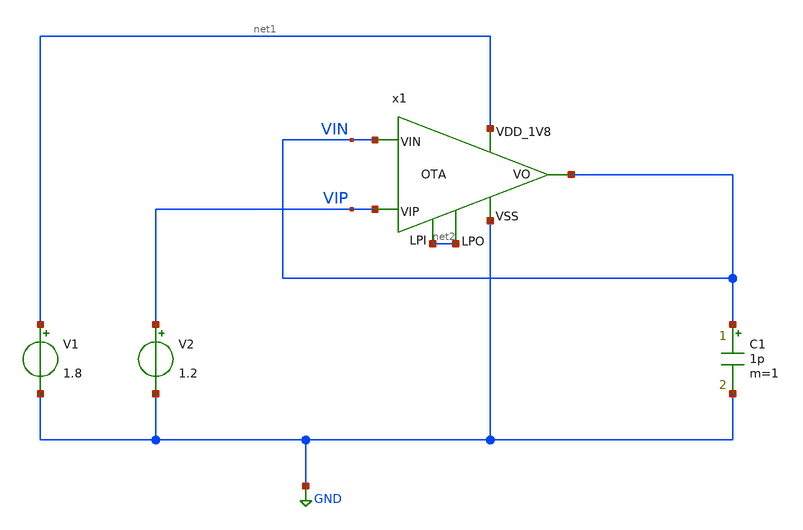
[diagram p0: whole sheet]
** sch_path: design/OTA_SKY130NM/TB_OTA.sch
**.subckt TB_OTA
V2 VIP GND 1.2
C1 VIN GND 1p m=1
V1 net1 GND 1.8
x1 net1 net2 net2 VIN VIN VIP GND OTA
**** begin user architecture code



* ngspice commands
.include corner.spi



**** end user architecture code
**.ends
.GLOBAL GND
.end
